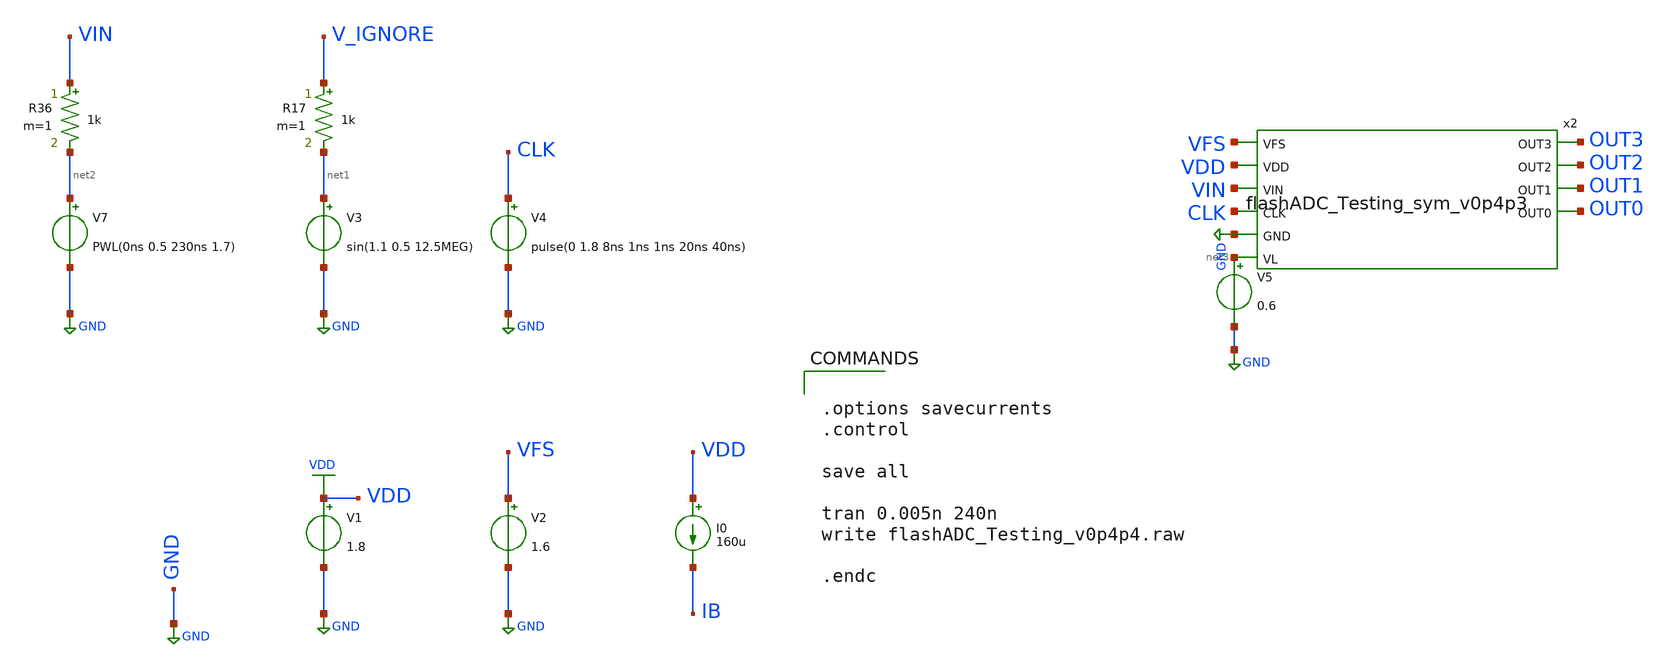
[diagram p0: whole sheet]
** sch_path: flashADC/xschem/flashADC_Testing_v0p4p4.sch
.lib $::SKYWATER_MODELS/sky130.lib.spice tt
.include $::SKYWATER_STDCELLS/sky130_fd_sc_hd.spice

**.subckt flashADC_Testing_v0p4p4
V3 net1 GND sin(1.1 0.5 12.5MEG)
V4 CLK GND pulse(0 1.8 8ns 1ns 1ns 20ns 40ns)
V1 VDD GND 1.8
V2 VFS GND 1.6
R17 V_IGNORE net1 1k m=1
I0 VDD IB 160u
V5 net3 GND 0.6
V7 net2 GND PWL(0ns 0.5 230ns 1.7)
R36 VIN net2 1k m=1
x2 VFS OUT3 OUT2 OUT1 OUT0 VDD VIN CLK GND net3 flashADC_Testing_sym_v0p4p3
**** begin user architecture code


.options savecurrents
.control

save all

tran 0.005n 240n
write flashADC_Testing_v0p4p4.raw

.endc


**** end user architecture code
**.ends
.GLOBAL GND
.GLOBAL VDD
.end
